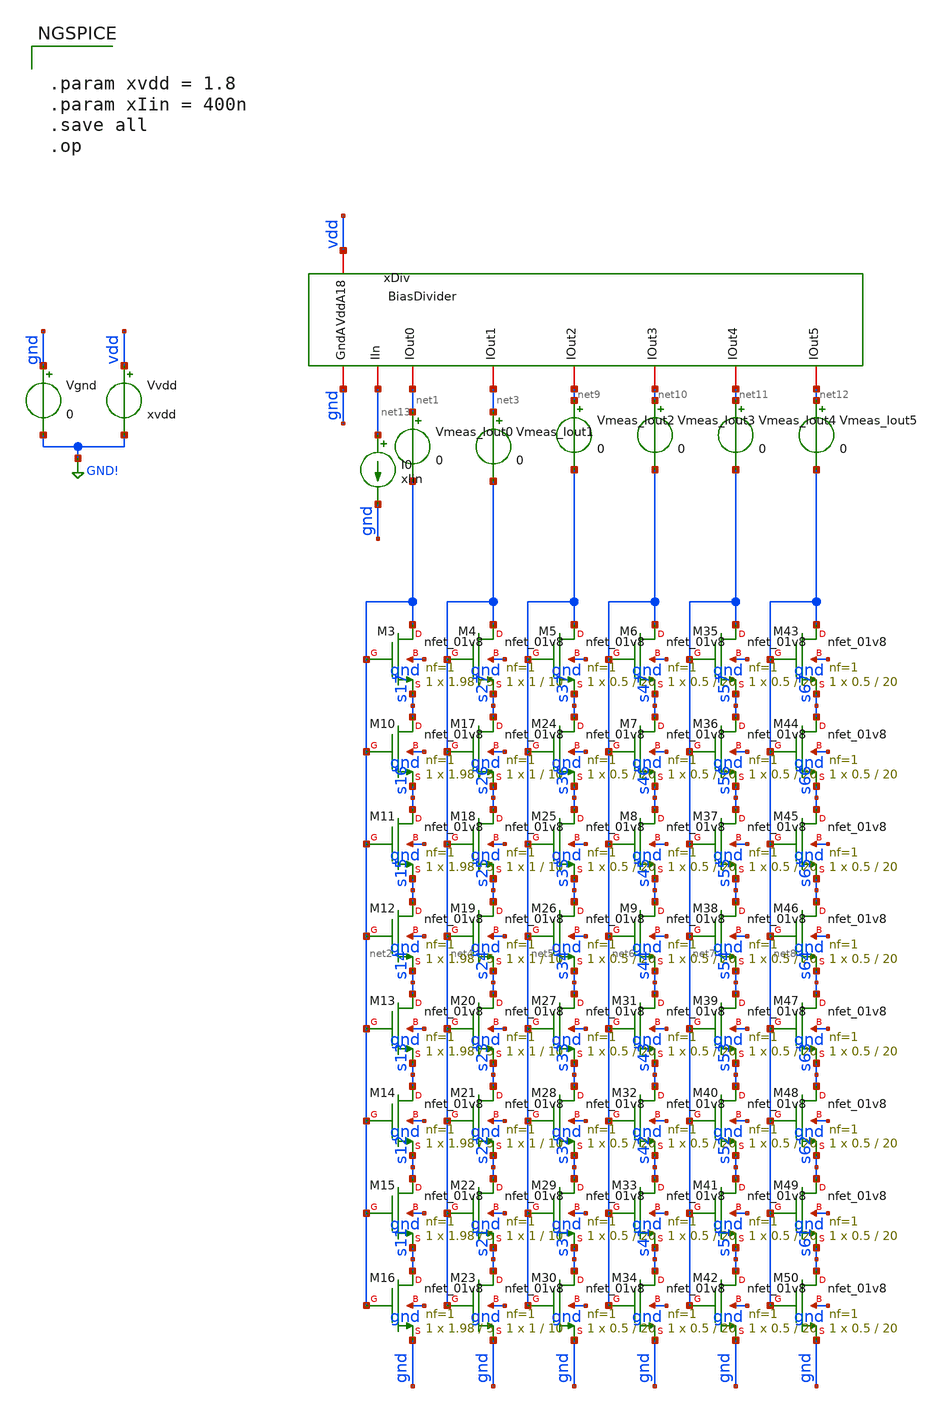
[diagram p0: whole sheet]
** sch_path: analog/klayout/production/final_merge_20260923/testbenches/cace/analog/xschem/tb_BiasDivider.sch
**.subckt tb_BiasDivider
Vgnd gnd GND! 0
.save i(vgnd)
Vvdd vdd GND! xvdd
.save i(vvdd)
I0 net13 gnd xIin
xDiv gnd vdd net13 net1 net3 net9 net10 net11 net12 BiasDivider
Vmeas_Iout0 net1 net2 0
.save i(vmeas_iout0)
Vmeas_Iout1 net3 net4 0
.save i(vmeas_iout1)
XM3 net2 net2 s17 gnd sky130_fd_pr__nfet_01v8 L=5 W=1.98 nf=1 ad='int((1 + 1)/2) * 1.98 / 1 * 0.29' as='int((1 + 2)/2) * 1.98 / 1 * 0.29'
+ pd='2*int((1 + 1)/2) * (1.98 / 1 + 0.29)' ps='2*int((1 + 2)/2) * (1.98 / 1 + 0.29)' nrd='0.29 / 1.98 '
+ nrs='0.29 / 1.98 ' sa=0 sb=0 sd=0 mult=1 m=1
XM4 net4 net4 s27 gnd sky130_fd_pr__nfet_01v8 L=10 W=1 nf=1 ad='int((1 + 1)/2) * 1 / 1 * 0.29' as='int((1 + 2)/2) * 1 / 1 * 0.29'
+ pd='2*int((1 + 1)/2) * (1 / 1 + 0.29)' ps='2*int((1 + 2)/2) * (1 / 1 + 0.29)' nrd='0.29 / 1 ' nrs='0.29 / 1 '
+ sa=0 sb=0 sd=0 mult=1 m=1
XM5 net5 net5 s37 gnd sky130_fd_pr__nfet_01v8 L=20 W=0.5 nf=1 ad='int((1 + 1)/2) * 0.5 / 1 * 0.29' as='int((1 + 2)/2) * 0.5 / 1 * 0.29'
+ pd='2*int((1 + 1)/2) * (0.5 / 1 + 0.29)' ps='2*int((1 + 2)/2) * (0.5 / 1 + 0.29)' nrd='0.29 / 0.5 ' nrs='0.29 / 0.5 '
+ sa=0 sb=0 sd=0 mult=1 m=1
XM10 s17 net2 s16 gnd sky130_fd_pr__nfet_01v8 L=5 W=1.98 nf=1 ad='int((1 + 1)/2) * 1.98 / 1 * 0.29' as='int((1 + 2)/2) * 1.98 / 1 * 0.29'
+ pd='2*int((1 + 1)/2) * (1.98 / 1 + 0.29)' ps='2*int((1 + 2)/2) * (1.98 / 1 + 0.29)' nrd='0.29 / 1.98 '
+ nrs='0.29 / 1.98 ' sa=0 sb=0 sd=0 mult=1 m=1
XM11 s16 net2 s15 gnd sky130_fd_pr__nfet_01v8 L=5 W=1.98 nf=1 ad='int((1 + 1)/2) * 1.98 / 1 * 0.29' as='int((1 + 2)/2) * 1.98 / 1 * 0.29'
+ pd='2*int((1 + 1)/2) * (1.98 / 1 + 0.29)' ps='2*int((1 + 2)/2) * (1.98 / 1 + 0.29)' nrd='0.29 / 1.98 '
+ nrs='0.29 / 1.98 ' sa=0 sb=0 sd=0 mult=1 m=1
XM12 s15 net2 s14 gnd sky130_fd_pr__nfet_01v8 L=5 W=1.98 nf=1 ad='int((1 + 1)/2) * 1.98 / 1 * 0.29' as='int((1 + 2)/2) * 1.98 / 1 * 0.29'
+ pd='2*int((1 + 1)/2) * (1.98 / 1 + 0.29)' ps='2*int((1 + 2)/2) * (1.98 / 1 + 0.29)' nrd='0.29 / 1.98 '
+ nrs='0.29 / 1.98 ' sa=0 sb=0 sd=0 mult=1 m=1
XM13 s14 net2 s13 gnd sky130_fd_pr__nfet_01v8 L=5 W=1.98 nf=1 ad='int((1 + 1)/2) * 1.98 / 1 * 0.29' as='int((1 + 2)/2) * 1.98 / 1 * 0.29'
+ pd='2*int((1 + 1)/2) * (1.98 / 1 + 0.29)' ps='2*int((1 + 2)/2) * (1.98 / 1 + 0.29)' nrd='0.29 / 1.98 '
+ nrs='0.29 / 1.98 ' sa=0 sb=0 sd=0 mult=1 m=1
XM14 s13 net2 s12 gnd sky130_fd_pr__nfet_01v8 L=5 W=1.98 nf=1 ad='int((1 + 1)/2) * 1.98 / 1 * 0.29' as='int((1 + 2)/2) * 1.98 / 1 * 0.29'
+ pd='2*int((1 + 1)/2) * (1.98 / 1 + 0.29)' ps='2*int((1 + 2)/2) * (1.98 / 1 + 0.29)' nrd='0.29 / 1.98 '
+ nrs='0.29 / 1.98 ' sa=0 sb=0 sd=0 mult=1 m=1
XM15 s12 net2 s11 gnd sky130_fd_pr__nfet_01v8 L=5 W=1.98 nf=1 ad='int((1 + 1)/2) * 1.98 / 1 * 0.29' as='int((1 + 2)/2) * 1.98 / 1 * 0.29'
+ pd='2*int((1 + 1)/2) * (1.98 / 1 + 0.29)' ps='2*int((1 + 2)/2) * (1.98 / 1 + 0.29)' nrd='0.29 / 1.98 '
+ nrs='0.29 / 1.98 ' sa=0 sb=0 sd=0 mult=1 m=1
XM16 s11 net2 gnd gnd sky130_fd_pr__nfet_01v8 L=5 W=1.98 nf=1 ad='int((1 + 1)/2) * 1.98 / 1 * 0.29' as='int((1 + 2)/2) * 1.98 / 1 * 0.29'
+ pd='2*int((1 + 1)/2) * (1.98 / 1 + 0.29)' ps='2*int((1 + 2)/2) * (1.98 / 1 + 0.29)' nrd='0.29 / 1.98 '
+ nrs='0.29 / 1.98 ' sa=0 sb=0 sd=0 mult=1 m=1
XM17 s27 net4 s26 gnd sky130_fd_pr__nfet_01v8 L=10 W=1 nf=1 ad='int((1 + 1)/2) * 1 / 1 * 0.29' as='int((1 + 2)/2) * 1 / 1 * 0.29'
+ pd='2*int((1 + 1)/2) * (1 / 1 + 0.29)' ps='2*int((1 + 2)/2) * (1 / 1 + 0.29)' nrd='0.29 / 1 ' nrs='0.29 / 1 '
+ sa=0 sb=0 sd=0 mult=1 m=1
XM18 s26 net4 s25 gnd sky130_fd_pr__nfet_01v8 L=10 W=1 nf=1 ad='int((1 + 1)/2) * 1 / 1 * 0.29' as='int((1 + 2)/2) * 1 / 1 * 0.29'
+ pd='2*int((1 + 1)/2) * (1 / 1 + 0.29)' ps='2*int((1 + 2)/2) * (1 / 1 + 0.29)' nrd='0.29 / 1 ' nrs='0.29 / 1 '
+ sa=0 sb=0 sd=0 mult=1 m=1
XM19 s25 net4 s24 gnd sky130_fd_pr__nfet_01v8 L=10 W=1 nf=1 ad='int((1 + 1)/2) * 1 / 1 * 0.29' as='int((1 + 2)/2) * 1 / 1 * 0.29'
+ pd='2*int((1 + 1)/2) * (1 / 1 + 0.29)' ps='2*int((1 + 2)/2) * (1 / 1 + 0.29)' nrd='0.29 / 1 ' nrs='0.29 / 1 '
+ sa=0 sb=0 sd=0 mult=1 m=1
XM20 s24 net4 s23 gnd sky130_fd_pr__nfet_01v8 L=10 W=1 nf=1 ad='int((1 + 1)/2) * 1 / 1 * 0.29' as='int((1 + 2)/2) * 1 / 1 * 0.29'
+ pd='2*int((1 + 1)/2) * (1 / 1 + 0.29)' ps='2*int((1 + 2)/2) * (1 / 1 + 0.29)' nrd='0.29 / 1 ' nrs='0.29 / 1 '
+ sa=0 sb=0 sd=0 mult=1 m=1
XM21 s23 net4 s22 gnd sky130_fd_pr__nfet_01v8 L=10 W=1 nf=1 ad='int((1 + 1)/2) * 1 / 1 * 0.29' as='int((1 + 2)/2) * 1 / 1 * 0.29'
+ pd='2*int((1 + 1)/2) * (1 / 1 + 0.29)' ps='2*int((1 + 2)/2) * (1 / 1 + 0.29)' nrd='0.29 / 1 ' nrs='0.29 / 1 '
+ sa=0 sb=0 sd=0 mult=1 m=1
XM22 s22 net4 s21 gnd sky130_fd_pr__nfet_01v8 L=10 W=1 nf=1 ad='int((1 + 1)/2) * 1 / 1 * 0.29' as='int((1 + 2)/2) * 1 / 1 * 0.29'
+ pd='2*int((1 + 1)/2) * (1 / 1 + 0.29)' ps='2*int((1 + 2)/2) * (1 / 1 + 0.29)' nrd='0.29 / 1 ' nrs='0.29 / 1 '
+ sa=0 sb=0 sd=0 mult=1 m=1
XM23 s21 net4 gnd gnd sky130_fd_pr__nfet_01v8 L=10 W=1 nf=1 ad='int((1 + 1)/2) * 1 / 1 * 0.29' as='int((1 + 2)/2) * 1 / 1 * 0.29'
+ pd='2*int((1 + 1)/2) * (1 / 1 + 0.29)' ps='2*int((1 + 2)/2) * (1 / 1 + 0.29)' nrd='0.29 / 1 ' nrs='0.29 / 1 '
+ sa=0 sb=0 sd=0 mult=1 m=1
XM24 s37 net5 s36 gnd sky130_fd_pr__nfet_01v8 L=20 W=0.5 nf=1 ad='int((1 + 1)/2) * 0.5 / 1 * 0.29' as='int((1 + 2)/2) * 0.5 / 1 * 0.29'
+ pd='2*int((1 + 1)/2) * (0.5 / 1 + 0.29)' ps='2*int((1 + 2)/2) * (0.5 / 1 + 0.29)' nrd='0.29 / 0.5 ' nrs='0.29 / 0.5 '
+ sa=0 sb=0 sd=0 mult=1 m=1
XM25 s36 net5 s35 gnd sky130_fd_pr__nfet_01v8 L=20 W=0.5 nf=1 ad='int((1 + 1)/2) * 0.5 / 1 * 0.29' as='int((1 + 2)/2) * 0.5 / 1 * 0.29'
+ pd='2*int((1 + 1)/2) * (0.5 / 1 + 0.29)' ps='2*int((1 + 2)/2) * (0.5 / 1 + 0.29)' nrd='0.29 / 0.5 ' nrs='0.29 / 0.5 '
+ sa=0 sb=0 sd=0 mult=1 m=1
XM26 s35 net5 s34 gnd sky130_fd_pr__nfet_01v8 L=20 W=0.5 nf=1 ad='int((1 + 1)/2) * 0.5 / 1 * 0.29' as='int((1 + 2)/2) * 0.5 / 1 * 0.29'
+ pd='2*int((1 + 1)/2) * (0.5 / 1 + 0.29)' ps='2*int((1 + 2)/2) * (0.5 / 1 + 0.29)' nrd='0.29 / 0.5 ' nrs='0.29 / 0.5 '
+ sa=0 sb=0 sd=0 mult=1 m=1
XM27 s34 net5 s33 gnd sky130_fd_pr__nfet_01v8 L=20 W=0.5 nf=1 ad='int((1 + 1)/2) * 0.5 / 1 * 0.29' as='int((1 + 2)/2) * 0.5 / 1 * 0.29'
+ pd='2*int((1 + 1)/2) * (0.5 / 1 + 0.29)' ps='2*int((1 + 2)/2) * (0.5 / 1 + 0.29)' nrd='0.29 / 0.5 ' nrs='0.29 / 0.5 '
+ sa=0 sb=0 sd=0 mult=1 m=1
XM28 s33 net5 s32 gnd sky130_fd_pr__nfet_01v8 L=20 W=0.5 nf=1 ad='int((1 + 1)/2) * 0.5 / 1 * 0.29' as='int((1 + 2)/2) * 0.5 / 1 * 0.29'
+ pd='2*int((1 + 1)/2) * (0.5 / 1 + 0.29)' ps='2*int((1 + 2)/2) * (0.5 / 1 + 0.29)' nrd='0.29 / 0.5 ' nrs='0.29 / 0.5 '
+ sa=0 sb=0 sd=0 mult=1 m=1
XM29 s32 net5 s31 gnd sky130_fd_pr__nfet_01v8 L=20 W=0.5 nf=1 ad='int((1 + 1)/2) * 0.5 / 1 * 0.29' as='int((1 + 2)/2) * 0.5 / 1 * 0.29'
+ pd='2*int((1 + 1)/2) * (0.5 / 1 + 0.29)' ps='2*int((1 + 2)/2) * (0.5 / 1 + 0.29)' nrd='0.29 / 0.5 ' nrs='0.29 / 0.5 '
+ sa=0 sb=0 sd=0 mult=1 m=1
XM30 s31 net5 gnd gnd sky130_fd_pr__nfet_01v8 L=20 W=0.5 nf=1 ad='int((1 + 1)/2) * 0.5 / 1 * 0.29' as='int((1 + 2)/2) * 0.5 / 1 * 0.29'
+ pd='2*int((1 + 1)/2) * (0.5 / 1 + 0.29)' ps='2*int((1 + 2)/2) * (0.5 / 1 + 0.29)' nrd='0.29 / 0.5 ' nrs='0.29 / 0.5 '
+ sa=0 sb=0 sd=0 mult=1 m=1
XM6 net6 net6 s47 gnd sky130_fd_pr__nfet_01v8 L=20 W=0.5 nf=1 ad='int((1 + 1)/2) * 0.5 / 1 * 0.29' as='int((1 + 2)/2) * 0.5 / 1 * 0.29'
+ pd='2*int((1 + 1)/2) * (0.5 / 1 + 0.29)' ps='2*int((1 + 2)/2) * (0.5 / 1 + 0.29)' nrd='0.29 / 0.5 ' nrs='0.29 / 0.5 '
+ sa=0 sb=0 sd=0 mult=1 m=1
XM7 s47 net6 s46 gnd sky130_fd_pr__nfet_01v8 L=20 W=0.5 nf=1 ad='int((1 + 1)/2) * 0.5 / 1 * 0.29' as='int((1 + 2)/2) * 0.5 / 1 * 0.29'
+ pd='2*int((1 + 1)/2) * (0.5 / 1 + 0.29)' ps='2*int((1 + 2)/2) * (0.5 / 1 + 0.29)' nrd='0.29 / 0.5 ' nrs='0.29 / 0.5 '
+ sa=0 sb=0 sd=0 mult=1 m=1
XM8 s46 net6 s45 gnd sky130_fd_pr__nfet_01v8 L=20 W=0.5 nf=1 ad='int((1 + 1)/2) * 0.5 / 1 * 0.29' as='int((1 + 2)/2) * 0.5 / 1 * 0.29'
+ pd='2*int((1 + 1)/2) * (0.5 / 1 + 0.29)' ps='2*int((1 + 2)/2) * (0.5 / 1 + 0.29)' nrd='0.29 / 0.5 ' nrs='0.29 / 0.5 '
+ sa=0 sb=0 sd=0 mult=1 m=1
XM9 s45 net6 s44 gnd sky130_fd_pr__nfet_01v8 L=20 W=0.5 nf=1 ad='int((1 + 1)/2) * 0.5 / 1 * 0.29' as='int((1 + 2)/2) * 0.5 / 1 * 0.29'
+ pd='2*int((1 + 1)/2) * (0.5 / 1 + 0.29)' ps='2*int((1 + 2)/2) * (0.5 / 1 + 0.29)' nrd='0.29 / 0.5 ' nrs='0.29 / 0.5 '
+ sa=0 sb=0 sd=0 mult=1 m=1
XM31 s44 net6 s43 gnd sky130_fd_pr__nfet_01v8 L=20 W=0.5 nf=1 ad='int((1 + 1)/2) * 0.5 / 1 * 0.29' as='int((1 + 2)/2) * 0.5 / 1 * 0.29'
+ pd='2*int((1 + 1)/2) * (0.5 / 1 + 0.29)' ps='2*int((1 + 2)/2) * (0.5 / 1 + 0.29)' nrd='0.29 / 0.5 ' nrs='0.29 / 0.5 '
+ sa=0 sb=0 sd=0 mult=1 m=1
XM32 s43 net6 s42 gnd sky130_fd_pr__nfet_01v8 L=20 W=0.5 nf=1 ad='int((1 + 1)/2) * 0.5 / 1 * 0.29' as='int((1 + 2)/2) * 0.5 / 1 * 0.29'
+ pd='2*int((1 + 1)/2) * (0.5 / 1 + 0.29)' ps='2*int((1 + 2)/2) * (0.5 / 1 + 0.29)' nrd='0.29 / 0.5 ' nrs='0.29 / 0.5 '
+ sa=0 sb=0 sd=0 mult=1 m=1
XM33 s42 net6 s41 gnd sky130_fd_pr__nfet_01v8 L=20 W=0.5 nf=1 ad='int((1 + 1)/2) * 0.5 / 1 * 0.29' as='int((1 + 2)/2) * 0.5 / 1 * 0.29'
+ pd='2*int((1 + 1)/2) * (0.5 / 1 + 0.29)' ps='2*int((1 + 2)/2) * (0.5 / 1 + 0.29)' nrd='0.29 / 0.5 ' nrs='0.29 / 0.5 '
+ sa=0 sb=0 sd=0 mult=1 m=1
XM34 s41 net6 gnd gnd sky130_fd_pr__nfet_01v8 L=20 W=0.5 nf=1 ad='int((1 + 1)/2) * 0.5 / 1 * 0.29' as='int((1 + 2)/2) * 0.5 / 1 * 0.29'
+ pd='2*int((1 + 1)/2) * (0.5 / 1 + 0.29)' ps='2*int((1 + 2)/2) * (0.5 / 1 + 0.29)' nrd='0.29 / 0.5 ' nrs='0.29 / 0.5 '
+ sa=0 sb=0 sd=0 mult=1 m=1
XM35 net7 net7 s57 gnd sky130_fd_pr__nfet_01v8 L=20 W=0.5 nf=1 ad='int((1 + 1)/2) * 0.5 / 1 * 0.29' as='int((1 + 2)/2) * 0.5 / 1 * 0.29'
+ pd='2*int((1 + 1)/2) * (0.5 / 1 + 0.29)' ps='2*int((1 + 2)/2) * (0.5 / 1 + 0.29)' nrd='0.29 / 0.5 ' nrs='0.29 / 0.5 '
+ sa=0 sb=0 sd=0 mult=1 m=1
XM36 s57 net7 s56 gnd sky130_fd_pr__nfet_01v8 L=20 W=0.5 nf=1 ad='int((1 + 1)/2) * 0.5 / 1 * 0.29' as='int((1 + 2)/2) * 0.5 / 1 * 0.29'
+ pd='2*int((1 + 1)/2) * (0.5 / 1 + 0.29)' ps='2*int((1 + 2)/2) * (0.5 / 1 + 0.29)' nrd='0.29 / 0.5 ' nrs='0.29 / 0.5 '
+ sa=0 sb=0 sd=0 mult=1 m=1
XM37 s56 net7 s55 gnd sky130_fd_pr__nfet_01v8 L=20 W=0.5 nf=1 ad='int((1 + 1)/2) * 0.5 / 1 * 0.29' as='int((1 + 2)/2) * 0.5 / 1 * 0.29'
+ pd='2*int((1 + 1)/2) * (0.5 / 1 + 0.29)' ps='2*int((1 + 2)/2) * (0.5 / 1 + 0.29)' nrd='0.29 / 0.5 ' nrs='0.29 / 0.5 '
+ sa=0 sb=0 sd=0 mult=1 m=1
XM38 s55 net7 s54 gnd sky130_fd_pr__nfet_01v8 L=20 W=0.5 nf=1 ad='int((1 + 1)/2) * 0.5 / 1 * 0.29' as='int((1 + 2)/2) * 0.5 / 1 * 0.29'
+ pd='2*int((1 + 1)/2) * (0.5 / 1 + 0.29)' ps='2*int((1 + 2)/2) * (0.5 / 1 + 0.29)' nrd='0.29 / 0.5 ' nrs='0.29 / 0.5 '
+ sa=0 sb=0 sd=0 mult=1 m=1
XM39 s54 net7 s53 gnd sky130_fd_pr__nfet_01v8 L=20 W=0.5 nf=1 ad='int((1 + 1)/2) * 0.5 / 1 * 0.29' as='int((1 + 2)/2) * 0.5 / 1 * 0.29'
+ pd='2*int((1 + 1)/2) * (0.5 / 1 + 0.29)' ps='2*int((1 + 2)/2) * (0.5 / 1 + 0.29)' nrd='0.29 / 0.5 ' nrs='0.29 / 0.5 '
+ sa=0 sb=0 sd=0 mult=1 m=1
XM40 s53 net7 s52 gnd sky130_fd_pr__nfet_01v8 L=20 W=0.5 nf=1 ad='int((1 + 1)/2) * 0.5 / 1 * 0.29' as='int((1 + 2)/2) * 0.5 / 1 * 0.29'
+ pd='2*int((1 + 1)/2) * (0.5 / 1 + 0.29)' ps='2*int((1 + 2)/2) * (0.5 / 1 + 0.29)' nrd='0.29 / 0.5 ' nrs='0.29 / 0.5 '
+ sa=0 sb=0 sd=0 mult=1 m=1
XM41 s52 net7 s51 gnd sky130_fd_pr__nfet_01v8 L=20 W=0.5 nf=1 ad='int((1 + 1)/2) * 0.5 / 1 * 0.29' as='int((1 + 2)/2) * 0.5 / 1 * 0.29'
+ pd='2*int((1 + 1)/2) * (0.5 / 1 + 0.29)' ps='2*int((1 + 2)/2) * (0.5 / 1 + 0.29)' nrd='0.29 / 0.5 ' nrs='0.29 / 0.5 '
+ sa=0 sb=0 sd=0 mult=1 m=1
XM42 s51 net7 gnd gnd sky130_fd_pr__nfet_01v8 L=20 W=0.5 nf=1 ad='int((1 + 1)/2) * 0.5 / 1 * 0.29' as='int((1 + 2)/2) * 0.5 / 1 * 0.29'
+ pd='2*int((1 + 1)/2) * (0.5 / 1 + 0.29)' ps='2*int((1 + 2)/2) * (0.5 / 1 + 0.29)' nrd='0.29 / 0.5 ' nrs='0.29 / 0.5 '
+ sa=0 sb=0 sd=0 mult=1 m=1
XM43 net8 net8 s67 gnd sky130_fd_pr__nfet_01v8 L=20 W=0.5 nf=1 ad='int((1 + 1)/2) * 0.5 / 1 * 0.29' as='int((1 + 2)/2) * 0.5 / 1 * 0.29'
+ pd='2*int((1 + 1)/2) * (0.5 / 1 + 0.29)' ps='2*int((1 + 2)/2) * (0.5 / 1 + 0.29)' nrd='0.29 / 0.5 ' nrs='0.29 / 0.5 '
+ sa=0 sb=0 sd=0 mult=1 m=1
XM44 s67 net8 s66 gnd sky130_fd_pr__nfet_01v8 L=20 W=0.5 nf=1 ad='int((1 + 1)/2) * 0.5 / 1 * 0.29' as='int((1 + 2)/2) * 0.5 / 1 * 0.29'
+ pd='2*int((1 + 1)/2) * (0.5 / 1 + 0.29)' ps='2*int((1 + 2)/2) * (0.5 / 1 + 0.29)' nrd='0.29 / 0.5 ' nrs='0.29 / 0.5 '
+ sa=0 sb=0 sd=0 mult=1 m=1
XM45 s66 net8 s65 gnd sky130_fd_pr__nfet_01v8 L=20 W=0.5 nf=1 ad='int((1 + 1)/2) * 0.5 / 1 * 0.29' as='int((1 + 2)/2) * 0.5 / 1 * 0.29'
+ pd='2*int((1 + 1)/2) * (0.5 / 1 + 0.29)' ps='2*int((1 + 2)/2) * (0.5 / 1 + 0.29)' nrd='0.29 / 0.5 ' nrs='0.29 / 0.5 '
+ sa=0 sb=0 sd=0 mult=1 m=1
XM46 s65 net8 s64 gnd sky130_fd_pr__nfet_01v8 L=20 W=0.5 nf=1 ad='int((1 + 1)/2) * 0.5 / 1 * 0.29' as='int((1 + 2)/2) * 0.5 / 1 * 0.29'
+ pd='2*int((1 + 1)/2) * (0.5 / 1 + 0.29)' ps='2*int((1 + 2)/2) * (0.5 / 1 + 0.29)' nrd='0.29 / 0.5 ' nrs='0.29 / 0.5 '
+ sa=0 sb=0 sd=0 mult=1 m=1
XM47 s64 net8 s63 gnd sky130_fd_pr__nfet_01v8 L=20 W=0.5 nf=1 ad='int((1 + 1)/2) * 0.5 / 1 * 0.29' as='int((1 + 2)/2) * 0.5 / 1 * 0.29'
+ pd='2*int((1 + 1)/2) * (0.5 / 1 + 0.29)' ps='2*int((1 + 2)/2) * (0.5 / 1 + 0.29)' nrd='0.29 / 0.5 ' nrs='0.29 / 0.5 '
+ sa=0 sb=0 sd=0 mult=1 m=1
XM48 s63 net8 s62 gnd sky130_fd_pr__nfet_01v8 L=20 W=0.5 nf=1 ad='int((1 + 1)/2) * 0.5 / 1 * 0.29' as='int((1 + 2)/2) * 0.5 / 1 * 0.29'
+ pd='2*int((1 + 1)/2) * (0.5 / 1 + 0.29)' ps='2*int((1 + 2)/2) * (0.5 / 1 + 0.29)' nrd='0.29 / 0.5 ' nrs='0.29 / 0.5 '
+ sa=0 sb=0 sd=0 mult=1 m=1
XM49 s62 net8 s61 gnd sky130_fd_pr__nfet_01v8 L=20 W=0.5 nf=1 ad='int((1 + 1)/2) * 0.5 / 1 * 0.29' as='int((1 + 2)/2) * 0.5 / 1 * 0.29'
+ pd='2*int((1 + 1)/2) * (0.5 / 1 + 0.29)' ps='2*int((1 + 2)/2) * (0.5 / 1 + 0.29)' nrd='0.29 / 0.5 ' nrs='0.29 / 0.5 '
+ sa=0 sb=0 sd=0 mult=1 m=1
XM50 s61 net8 gnd gnd sky130_fd_pr__nfet_01v8 L=20 W=0.5 nf=1 ad='int((1 + 1)/2) * 0.5 / 1 * 0.29' as='int((1 + 2)/2) * 0.5 / 1 * 0.29'
+ pd='2*int((1 + 1)/2) * (0.5 / 1 + 0.29)' ps='2*int((1 + 2)/2) * (0.5 / 1 + 0.29)' nrd='0.29 / 0.5 ' nrs='0.29 / 0.5 '
+ sa=0 sb=0 sd=0 mult=1 m=1
Vmeas_Iout2 net9 net5 0
.save i(vmeas_iout2)
Vmeas_Iout3 net10 net6 0
.save i(vmeas_iout3)
Vmeas_Iout4 net11 net7 0
.save i(vmeas_iout4)
Vmeas_Iout5 net12 net8 0
.save i(vmeas_iout5)
**** begin user architecture code

** opencircuitdesign pdks install
.lib $::SKYWATER_MODELS/sky130.lib.spice tt



.param xvdd = 1.8
.param xIin = 400n
.save all
.op


**** end user architecture code
**.ends
.GLOBAL GND!
.end
